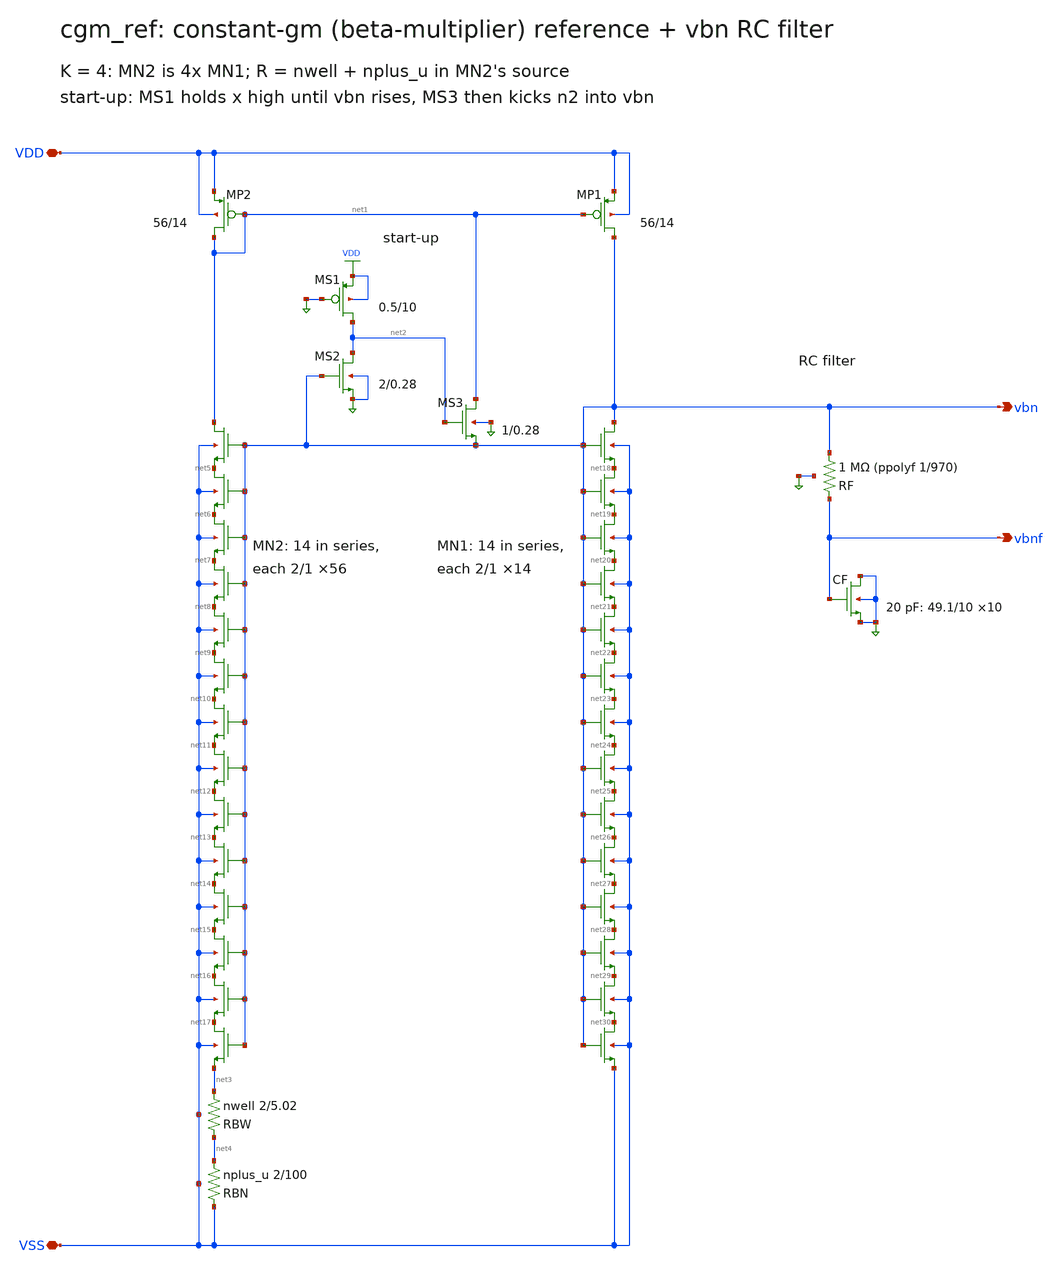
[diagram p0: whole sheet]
** sch_path: xschem/cgm_ref.sch
**.subckt cgm_ref VDD VSS vbn vbnf
*.iopin VDD
*.iopin VSS
*.opin vbn
*.opin vbnf
XMP2 net1 net1 VDD VDD pfet_03v3 L=14.0u W=56.0u nf=1 ad=28.0p as=28.0p pd=113.0u ps=113.0u nrd=0
+ nrs=0 sa=0 sb=0 sd=0 m=1
XMP1 vbn net1 VDD VDD pfet_03v3 L=14.0u W=56.0u nf=1 ad=28.0p as=28.0p pd=113.0u ps=113.0u nrd=0
+ nrs=0 sa=0 sb=0 sd=0 m=1
XMN2 net1 vbn net5 VSS nfet_03v3 L=1.0u W=2.0u nf=1 ad=1.0p as=1.0p pd=5.0u ps=5.0u nrd=0 nrs=0 sa=0
+ sb=0 sd=0 m=56
XMN2s1 net5 vbn net6 VSS nfet_03v3 L=1.0u W=2.0u nf=1 ad=1.0p as=1.0p pd=5.0u ps=5.0u nrd=0 nrs=0
+ sa=0 sb=0 sd=0 m=56
XMN2s2 net6 vbn net7 VSS nfet_03v3 L=1.0u W=2.0u nf=1 ad=1.0p as=1.0p pd=5.0u ps=5.0u nrd=0 nrs=0
+ sa=0 sb=0 sd=0 m=56
XMN2s3 net7 vbn net8 VSS nfet_03v3 L=1.0u W=2.0u nf=1 ad=1.0p as=1.0p pd=5.0u ps=5.0u nrd=0 nrs=0
+ sa=0 sb=0 sd=0 m=56
XMN2s4 net8 vbn net9 VSS nfet_03v3 L=1.0u W=2.0u nf=1 ad=1.0p as=1.0p pd=5.0u ps=5.0u nrd=0 nrs=0
+ sa=0 sb=0 sd=0 m=56
XMN2s5 net9 vbn net10 VSS nfet_03v3 L=1.0u W=2.0u nf=1 ad=1.0p as=1.0p pd=5.0u ps=5.0u nrd=0 nrs=0
+ sa=0 sb=0 sd=0 m=56
XMN2s6 net10 vbn net11 VSS nfet_03v3 L=1.0u W=2.0u nf=1 ad=1.0p as=1.0p pd=5.0u ps=5.0u nrd=0 nrs=0
+ sa=0 sb=0 sd=0 m=56
XMN2s7 net11 vbn net12 VSS nfet_03v3 L=1.0u W=2.0u nf=1 ad=1.0p as=1.0p pd=5.0u ps=5.0u nrd=0 nrs=0
+ sa=0 sb=0 sd=0 m=56
XMN2s8 net12 vbn net13 VSS nfet_03v3 L=1.0u W=2.0u nf=1 ad=1.0p as=1.0p pd=5.0u ps=5.0u nrd=0 nrs=0
+ sa=0 sb=0 sd=0 m=56
XMN2s9 net13 vbn net14 VSS nfet_03v3 L=1.0u W=2.0u nf=1 ad=1.0p as=1.0p pd=5.0u ps=5.0u nrd=0 nrs=0
+ sa=0 sb=0 sd=0 m=56
XMN2s10 net14 vbn net15 VSS nfet_03v3 L=1.0u W=2.0u nf=1 ad=1.0p as=1.0p pd=5.0u ps=5.0u nrd=0 nrs=0
+ sa=0 sb=0 sd=0 m=56
XMN2s11 net15 vbn net16 VSS nfet_03v3 L=1.0u W=2.0u nf=1 ad=1.0p as=1.0p pd=5.0u ps=5.0u nrd=0 nrs=0
+ sa=0 sb=0 sd=0 m=56
XMN2s12 net16 vbn net17 VSS nfet_03v3 L=1.0u W=2.0u nf=1 ad=1.0p as=1.0p pd=5.0u ps=5.0u nrd=0 nrs=0
+ sa=0 sb=0 sd=0 m=56
XMN2s13 net17 vbn net3 VSS nfet_03v3 L=1.0u W=2.0u nf=1 ad=1.0p as=1.0p pd=5.0u ps=5.0u nrd=0 nrs=0
+ sa=0 sb=0 sd=0 m=56
XMN1 vbn vbn net18 VSS nfet_03v3 L=1.0u W=2.0u nf=1 ad=1.0p as=1.0p pd=5.0u ps=5.0u nrd=0 nrs=0 sa=0
+ sb=0 sd=0 m=14
XMN1s1 net18 vbn net19 VSS nfet_03v3 L=1.0u W=2.0u nf=1 ad=1.0p as=1.0p pd=5.0u ps=5.0u nrd=0 nrs=0
+ sa=0 sb=0 sd=0 m=14
XMN1s2 net19 vbn net20 VSS nfet_03v3 L=1.0u W=2.0u nf=1 ad=1.0p as=1.0p pd=5.0u ps=5.0u nrd=0 nrs=0
+ sa=0 sb=0 sd=0 m=14
XMN1s3 net20 vbn net21 VSS nfet_03v3 L=1.0u W=2.0u nf=1 ad=1.0p as=1.0p pd=5.0u ps=5.0u nrd=0 nrs=0
+ sa=0 sb=0 sd=0 m=14
XMN1s4 net21 vbn net22 VSS nfet_03v3 L=1.0u W=2.0u nf=1 ad=1.0p as=1.0p pd=5.0u ps=5.0u nrd=0 nrs=0
+ sa=0 sb=0 sd=0 m=14
XMN1s5 net22 vbn net23 VSS nfet_03v3 L=1.0u W=2.0u nf=1 ad=1.0p as=1.0p pd=5.0u ps=5.0u nrd=0 nrs=0
+ sa=0 sb=0 sd=0 m=14
XMN1s6 net23 vbn net24 VSS nfet_03v3 L=1.0u W=2.0u nf=1 ad=1.0p as=1.0p pd=5.0u ps=5.0u nrd=0 nrs=0
+ sa=0 sb=0 sd=0 m=14
XMN1s7 net24 vbn net25 VSS nfet_03v3 L=1.0u W=2.0u nf=1 ad=1.0p as=1.0p pd=5.0u ps=5.0u nrd=0 nrs=0
+ sa=0 sb=0 sd=0 m=14
XMN1s8 net25 vbn net26 VSS nfet_03v3 L=1.0u W=2.0u nf=1 ad=1.0p as=1.0p pd=5.0u ps=5.0u nrd=0 nrs=0
+ sa=0 sb=0 sd=0 m=14
XMN1s9 net26 vbn net27 VSS nfet_03v3 L=1.0u W=2.0u nf=1 ad=1.0p as=1.0p pd=5.0u ps=5.0u nrd=0 nrs=0
+ sa=0 sb=0 sd=0 m=14
XMN1s10 net27 vbn net28 VSS nfet_03v3 L=1.0u W=2.0u nf=1 ad=1.0p as=1.0p pd=5.0u ps=5.0u nrd=0 nrs=0
+ sa=0 sb=0 sd=0 m=14
XMN1s11 net28 vbn net29 VSS nfet_03v3 L=1.0u W=2.0u nf=1 ad=1.0p as=1.0p pd=5.0u ps=5.0u nrd=0 nrs=0
+ sa=0 sb=0 sd=0 m=14
XMN1s12 net29 vbn net30 VSS nfet_03v3 L=1.0u W=2.0u nf=1 ad=1.0p as=1.0p pd=5.0u ps=5.0u nrd=0 nrs=0
+ sa=0 sb=0 sd=0 m=14
XMN1s13 net30 vbn VSS VSS nfet_03v3 L=1.0u W=2.0u nf=1 ad=1.0p as=1.0p pd=5.0u ps=5.0u nrd=0 nrs=0
+ sa=0 sb=0 sd=0 m=14
XMS1 net2 VSS VDD VDD pfet_03v3 L=10.0u W=0.5u nf=1 ad=0.25p as=0.25p pd=2.0u ps=2.0u nrd=0 nrs=0
+ sa=0 sb=0 sd=0 m=1
XMS2 net2 vbn VSS VSS nfet_03v3 L=0.28u W=2.0u nf=1 ad=1.0p as=1.0p pd=5.0u ps=5.0u nrd=0 nrs=0 sa=0
+ sb=0 sd=0 m=1
XMS3 net1 net2 vbn VSS nfet_03v3 L=0.28u W=1.0u nf=1 ad=0.5p as=0.5p pd=3.0u ps=3.0u nrd=0 nrs=0
+ sa=0 sb=0 sd=0 m=1
XRBW net3 net4 VSS nwell r_width=2.0e-6 r_length=5.023e-6 m=1
XRBN net4 VSS VSS nplus_u r_width=2.0e-6 r_length=100.0e-6 m=1
XRF vbn vbnf VSS ppolyf_u_1k r_width=1.0e-6 r_length=970.2289999999999e-6 m=1
XCF VSS vbnf VSS VSS nfet_03v3 L=10.0u W=49.14u nf=1 ad=24.57p as=24.57p pd=99.28u ps=99.28u nrd=0
+ nrs=0 sa=0 sb=0 sd=0 m=10
**.ends
.end
